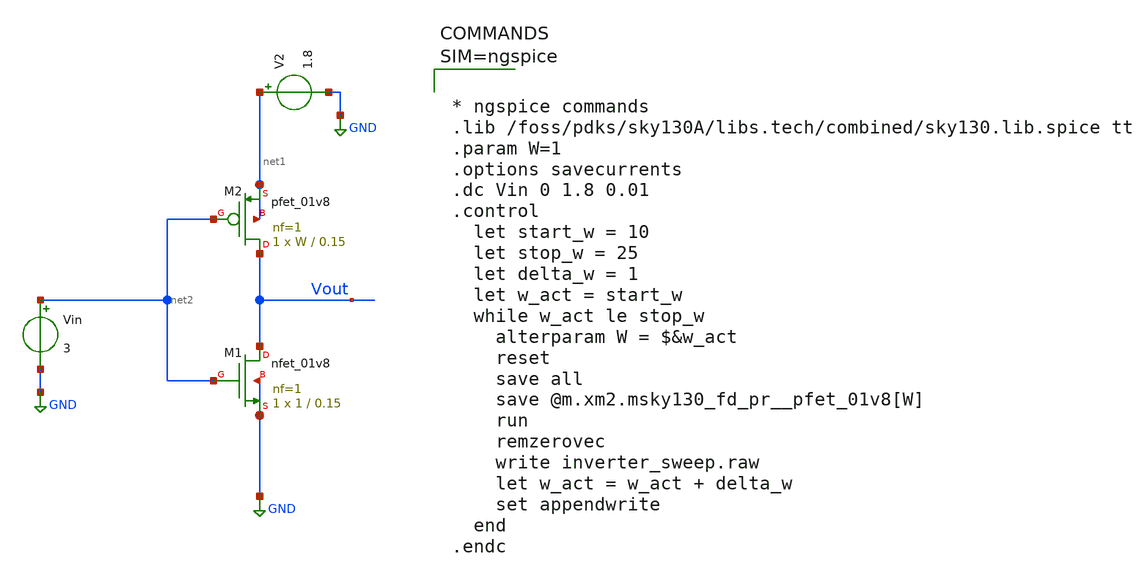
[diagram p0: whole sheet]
** sch_path: tt_um_emmersonv_tiq_adc/xschem/inverter_sweep.sch
**.subckt inverter_sweep
XM1 Vout net2 GND GND sky130_fd_pr__nfet_01v8 L=0.15 W=1 nf=1 ad='int((nf+1)/2) * W/nf * 0.29' as='int((nf+2)/2) * W/nf * 0.29'
+ pd='2*int((nf+1)/2) * (W/nf + 0.29)' ps='2*int((nf+2)/2) * (W/nf + 0.29)' nrd='0.29 / W' nrs='0.29 / W'
+ sa=0 sb=0 sd=0 mult=1 m=1
XM2 Vout net2 net1 net1 sky130_fd_pr__pfet_01v8 L=0.15 W=W nf=1 ad='int((nf+1)/2) * W/nf * 0.29' as='int((nf+2)/2) * W/nf * 0.29'
+ pd='2*int((nf+1)/2) * (W/nf + 0.29)' ps='2*int((nf+2)/2) * (W/nf + 0.29)' nrd='0.29 / W' nrs='0.29 / W'
+ sa=0 sb=0 sd=0 mult=1 m=1
Vin net2 GND 3
V2 net1 GND 1.8
**** begin user architecture code



* ngspice commands
.lib /foss/pdks/sky130A/libs.tech/combined/sky130.lib.spice tt
.param W=1
.options savecurrents
.dc Vin 0 1.8 0.01
.control
  let start_w = 10
  let stop_w = 25
  let delta_w = 1
  let w_act = start_w
  while w_act le stop_w
    alterparam W = $&w_act
    reset
    save all
    save @m.xm2.msky130_fd_pr__pfet_01v8[W]
    run
    remzerovec
    write inverter_sweep.raw
    let w_act = w_act + delta_w
    set appendwrite
  end
.endc



**** end user architecture code
**.ends
.GLOBAL GND
.end
